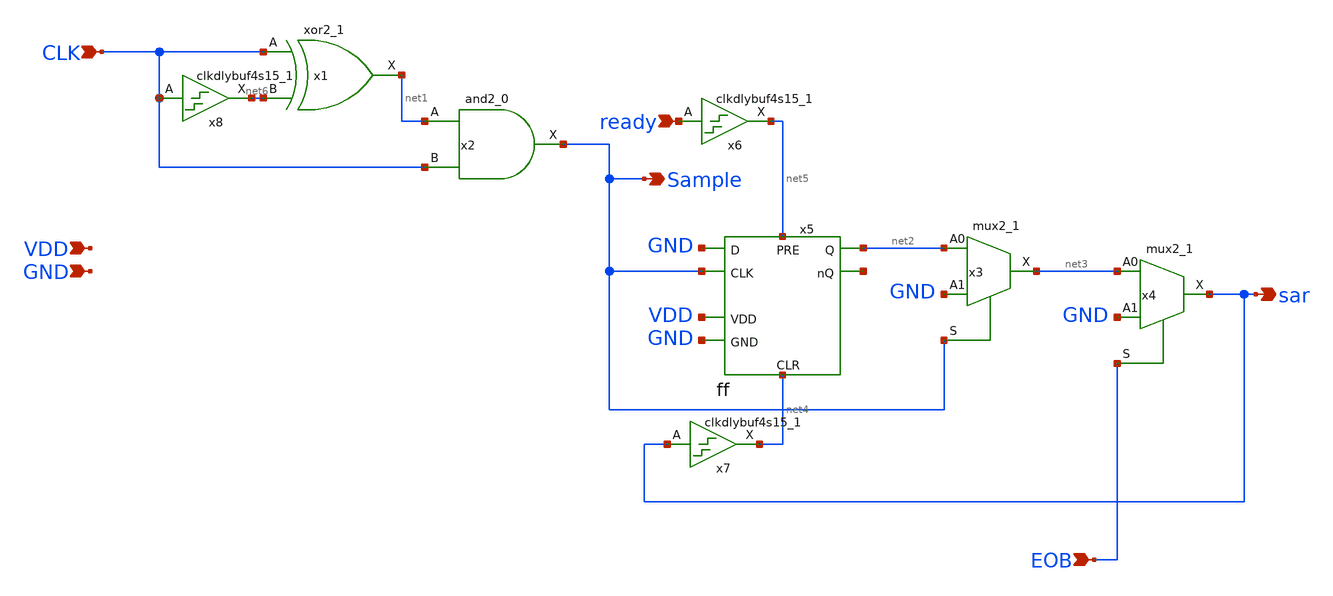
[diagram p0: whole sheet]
** sch_path: xschem/clkgen/clkgen.sch
**.subckt clkgen CLK ready EOB Sample sar VDD GND
*.ipin CLK
*.ipin ready
*.ipin EOB
*.opin Sample
*.opin sar
*.ipin VDD
*.ipin GND
x1 CLK net6 GND GND VDD VDD net1 sky130_fd_sc_hd__xor2_1
x2 net1 CLK GND GND VDD VDD Sample sky130_fd_sc_hd__and2_0
x3 net2 GND Sample GND GND VDD VDD net3 sky130_fd_sc_hd__mux2_1
x5 VDD GND net5 Sample net4 net2 GND net7 ff
x8 CLK GND GND VDD VDD net6 sky130_fd_sc_hd__clkdlybuf4s15_1
x6 ready GND GND VDD VDD net5 sky130_fd_sc_hd__clkdlybuf4s15_1
x7 sar GND GND VDD VDD net4 sky130_fd_sc_hd__clkdlybuf4s15_1
x4 net3 GND EOB GND GND VDD VDD sar sky130_fd_sc_hd__mux2_1
**.ends

* expanding   symbol:  ff.sym # of pins=8
** sym_path: xschem/ff.sym
** sch_path: xschem/ff.sch
.subckt ff VDD GND PRE CLK CLR Q D nQ
*.opin nQ
*.opin Q
*.ipin VDD
*.ipin GND
*.ipin D
*.ipin PRE
*.ipin CLR
*.ipin CLK
XM1 Q net1 GND GND sky130_fd_pr__nfet_01v8 L=0.15 W=1 nf=1 ad='int((nf+1)/2) * W/nf * 0.29' as='int((nf+2)/2) * W/nf * 0.29'
+ pd='2*int((nf+1)/2) * (W/nf + 0.29)' ps='2*int((nf+2)/2) * (W/nf + 0.29)' nrd='0.29 / W' nrs='0.29 / W'
+ sa=0 sb=0 sd=0 mult=1 m=1
XM2 Q net1 VDD VDD sky130_fd_pr__pfet_01v8 L=0.15 W=1 nf=1 ad='int((nf+1)/2) * W/nf * 0.29' as='int((nf+2)/2) * W/nf * 0.29'
+ pd='2*int((nf+1)/2) * (W/nf + 0.29)' ps='2*int((nf+2)/2) * (W/nf + 0.29)' nrd='0.29 / W' nrs='0.29 / W'
+ sa=0 sb=0 sd=0 mult=1 m=1
XM3 nQ Q GND GND sky130_fd_pr__nfet_01v8 L=0.15 W=1 nf=1 ad='int((nf+1)/2) * W/nf * 0.29' as='int((nf+2)/2) * W/nf * 0.29'
+ pd='2*int((nf+1)/2) * (W/nf + 0.29)' ps='2*int((nf+2)/2) * (W/nf + 0.29)' nrd='0.29 / W' nrs='0.29 / W'
+ sa=0 sb=0 sd=0 mult=1 m=1
XM4 nQ Q VDD VDD sky130_fd_pr__pfet_01v8 L=0.15 W=1 nf=1 ad='int((nf+1)/2) * W/nf * 0.29' as='int((nf+2)/2) * W/nf * 0.29'
+ pd='2*int((nf+1)/2) * (W/nf + 0.29)' ps='2*int((nf+2)/2) * (W/nf + 0.29)' nrd='0.29 / W' nrs='0.29 / W'
+ sa=0 sb=0 sd=0 mult=1 m=1
XM5 net1 net2 VDD VDD sky130_fd_pr__pfet_01v8 L=0.15 W=1 nf=1 ad='int((nf+1)/2) * W/nf * 0.29' as='int((nf+2)/2) * W/nf * 0.29'
+ pd='2*int((nf+1)/2) * (W/nf + 0.29)' ps='2*int((nf+2)/2) * (W/nf + 0.29)' nrd='0.29 / W' nrs='0.29 / W'
+ sa=0 sb=0 sd=0 mult=1 m=1
XM6 net1 PRE GND GND sky130_fd_pr__nfet_01v8 L=0.15 W=1 nf=1 ad='int((nf+1)/2) * W/nf * 0.29' as='int((nf+2)/2) * W/nf * 0.29'
+ pd='2*int((nf+1)/2) * (W/nf + 0.29)' ps='2*int((nf+2)/2) * (W/nf + 0.29)' nrd='0.29 / W' nrs='0.29 / W'
+ sa=0 sb=0 sd=0 mult=1 m=1
XM7 net1 PRE net3 VDD sky130_fd_pr__pfet_01v8 L=0.15 W=1 nf=1 ad='int((nf+1)/2) * W/nf * 0.29' as='int((nf+2)/2) * W/nf * 0.29'
+ pd='2*int((nf+1)/2) * (W/nf + 0.29)' ps='2*int((nf+2)/2) * (W/nf + 0.29)' nrd='0.29 / W' nrs='0.29 / W'
+ sa=0 sb=0 sd=0 mult=1 m=1
XM8 net3 net5 VDD VDD sky130_fd_pr__pfet_01v8 L=0.15 W=1 nf=1 ad='int((nf+1)/2) * W/nf * 0.29' as='int((nf+2)/2) * W/nf * 0.29'
+ pd='2*int((nf+1)/2) * (W/nf + 0.29)' ps='2*int((nf+2)/2) * (W/nf + 0.29)' nrd='0.29 / W' nrs='0.29 / W'
+ sa=0 sb=0 sd=0 mult=1 m=1
XM9 net1 CLK net4 GND sky130_fd_pr__nfet_01v8 L=0.15 W=1 nf=1 ad='int((nf+1)/2) * W/nf * 0.29' as='int((nf+2)/2) * W/nf * 0.29'
+ pd='2*int((nf+1)/2) * (W/nf + 0.29)' ps='2*int((nf+2)/2) * (W/nf + 0.29)' nrd='0.29 / W' nrs='0.29 / W'
+ sa=0 sb=0 sd=0 mult=1 m=1
XM10 net4 net5 GND GND sky130_fd_pr__nfet_01v8 L=0.15 W=1 nf=1 ad='int((nf+1)/2) * W/nf * 0.29' as='int((nf+2)/2) * W/nf * 0.29'
+ pd='2*int((nf+1)/2) * (W/nf + 0.29)' ps='2*int((nf+2)/2) * (W/nf + 0.29)' nrd='0.29 / W' nrs='0.29 / W'
+ sa=0 sb=0 sd=0 mult=1 m=1
XM11 net5 CLK VDD VDD sky130_fd_pr__pfet_01v8 L=0.15 W=1 nf=1 ad='int((nf+1)/2) * W/nf * 0.29' as='int((nf+2)/2) * W/nf * 0.29'
+ pd='2*int((nf+1)/2) * (W/nf + 0.29)' ps='2*int((nf+2)/2) * (W/nf + 0.29)' nrd='0.29 / W' nrs='0.29 / W'
+ sa=0 sb=0 sd=0 mult=1 m=1
XM12 net5 net7 net6 GND sky130_fd_pr__nfet_01v8 L=0.15 W=1 nf=1 ad='int((nf+1)/2) * W/nf * 0.29' as='int((nf+2)/2) * W/nf * 0.29'
+ pd='2*int((nf+1)/2) * (W/nf + 0.29)' ps='2*int((nf+2)/2) * (W/nf + 0.29)' nrd='0.29 / W' nrs='0.29 / W'
+ sa=0 sb=0 sd=0 mult=1 m=1
XM13 net6 CLK GND GND sky130_fd_pr__nfet_01v8 L=0.15 W=1 nf=1 ad='int((nf+1)/2) * W/nf * 0.29' as='int((nf+2)/2) * W/nf * 0.29'
+ pd='2*int((nf+1)/2) * (W/nf + 0.29)' ps='2*int((nf+2)/2) * (W/nf + 0.29)' nrd='0.29 / W' nrs='0.29 / W'
+ sa=0 sb=0 sd=0 mult=1 m=1
XM15 net7 D GND GND sky130_fd_pr__nfet_01v8 L=0.15 W=1 nf=1 ad='int((nf+1)/2) * W/nf * 0.29' as='int((nf+2)/2) * W/nf * 0.29'
+ pd='2*int((nf+1)/2) * (W/nf + 0.29)' ps='2*int((nf+2)/2) * (W/nf + 0.29)' nrd='0.29 / W' nrs='0.29 / W'
+ sa=0 sb=0 sd=0 mult=1 m=1
XM14 net7 CLK net8 VDD sky130_fd_pr__pfet_01v8 L=0.15 W=1 nf=1 ad='int((nf+1)/2) * W/nf * 0.29' as='int((nf+2)/2) * W/nf * 0.29'
+ pd='2*int((nf+1)/2) * (W/nf + 0.29)' ps='2*int((nf+2)/2) * (W/nf + 0.29)' nrd='0.29 / W' nrs='0.29 / W'
+ sa=0 sb=0 sd=0 mult=1 m=1
XM16 net8 D VDD VDD sky130_fd_pr__pfet_01v8 L=0.15 W=1 nf=1 ad='int((nf+1)/2) * W/nf * 0.29' as='int((nf+2)/2) * W/nf * 0.29'
+ pd='2*int((nf+1)/2) * (W/nf + 0.29)' ps='2*int((nf+2)/2) * (W/nf + 0.29)' nrd='0.29 / W' nrs='0.29 / W'
+ sa=0 sb=0 sd=0 mult=1 m=1
x2 net2 CLR Inverter
.ends


* expanding   symbol:  Inverter.sym # of pins=2
** sym_path: xschem/Inverter.sym
** sch_path: xschem/Inverter.sch
.subckt Inverter Vout Vin
*.ipin Vin
*.opin Vout
XM1 Vout Vin GND GND sky130_fd_pr__nfet_01v8 L=0.15 W=1 nf=1 ad='int((nf+1)/2) * W/nf * 0.29' as='int((nf+2)/2) * W/nf * 0.29'
+ pd='2*int((nf+1)/2) * (W/nf + 0.29)' ps='2*int((nf+2)/2) * (W/nf + 0.29)' nrd='0.29 / W' nrs='0.29 / W'
+ sa=0 sb=0 sd=0 mult=1 m=1
XM2 Vout Vin VDD VDD sky130_fd_pr__pfet_01v8 L=0.15 W=4 nf=1 ad='int((nf+1)/2) * W/nf * 0.29' as='int((nf+2)/2) * W/nf * 0.29'
+ pd='2*int((nf+1)/2) * (W/nf + 0.29)' ps='2*int((nf+2)/2) * (W/nf + 0.29)' nrd='0.29 / W' nrs='0.29 / W'
+ sa=0 sb=0 sd=0 mult=1 m=1
V1 VDD GND 1.8
.ends

.GLOBAL GND
.end
